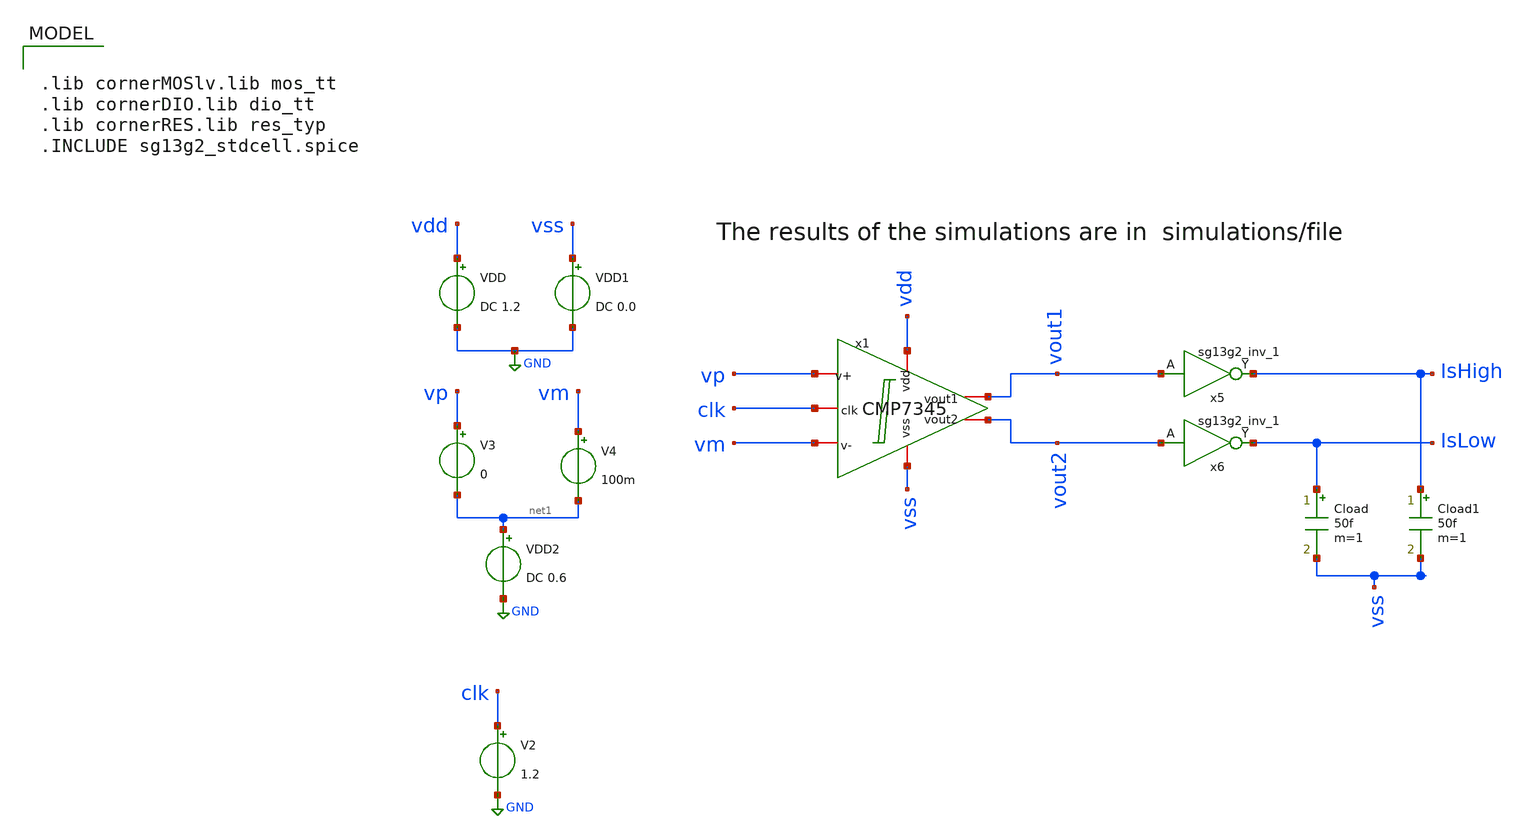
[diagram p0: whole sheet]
** sch_path: CMP7345-main/testbenches/dc/xschem/CMP7345_dc_tb.sch
**.subckt CMP7345_dc_tb
VDD vdd GND DC 1.2
Cload IsLow vss 50f m=1
x1 vdd vout1 vout2 vp vm clk vss CMP7345
VDD1 vss GND DC 0.0
Cload1 IsHigh vss 50f m=1
V2 clk GND 1.2
V3 vp net1 0
VDD2 net1 GND DC 0.6
x5 IsHigh vout1 VDD VSS sg13g2_inv_1
x6 IsLow vout2 VDD VSS sg13g2_inv_1
V4 vm net1 100m
**** begin user architecture code

.lib cornerMOSlv.lib mos_tt
.lib cornerDIO.lib dio_tt
.lib cornerRES.lib res_typ
.INCLUDE sg13g2_stdcell.spice




.options cshunt=20f
.options rseries=1
.control
op
echo " ---------------- Diff pair ----------------" > file
let ids1 = 8*@n.x1.x1.xmb1.nsg13_lv_nmos[ids]
echo Ids1 = $&ids1 >> file
let ids2 = 8*@n.x1.x1.xma1.nsg13_lv_nmos[ids]
echo Ids2 = $&ids2 >> file
let Vgs1 = @n.x1.x1.xmb1.nsg13_lv_nmos[vgs]
echo Vgs1 = $&vgs1 >> file
let Vgs2 = @n.x1.x1.xma1.nsg13_lv_nmos[vgs]
echo Vgs2 = $&vgs2 >> file
let Vth1 = @n.x1.x1.xmb1.nsg13_lv_nmos[vth]
echo Vth1 = $&vth1 >> file
let Vth2 = @n.x1.x1.xma1.nsg13_lv_nmos[vth]
echo Vth2 = $&vth2 >> file
let gm1 = 8*@n.x1.x1.xmb1.nsg13_lv_nmos[gm]
echo gm1 = $&gm1 >> file
let gm2 = 8*@n.x1.x1.xma1.nsg13_lv_nmos[gm]
echo gm2 = $&gm2 >> file
let cdd1 = 8*@n.x1.x1.xmb1.nsg13_lv_nmos[cdd]
echo cdd1 = $&cdd1 >> file
let cdd2 = 8*@n.x1.x1.xma1.nsg13_lv_nmos[cdd]
echo cdd2 = $&cdd2 >> file
let cgg1 = 8*@n.x1.x1.xmb1.nsg13_lv_nmos[cgg]
echo cgg1 = $&cgg1 >> file
let cgg2 = 8*@n.x1.x1.xma1.nsg13_lv_nmos[cgg]
echo cgg2 = $&cgg2 >> file
let css1 = 8*@n.x1.x1.xmb1.nsg13_lv_nmos[css]
echo css1 = $&css1 >> file
let css2 = 8*@n.x1.x1.xma1.nsg13_lv_nmos[css]
echo css2 = $&css2 >> file
echo " ---------------- Tail switch ----------------" >> file
let ids = @n.x1.xm7.nsg13_lv_nmos[ids]
echo Ids = $&ids >> file
let vgs = @n.x1.xm7.nsg13_lv_nmos[vgs]
echo Vgs = $&vgs >> file
let vth = @n.x1.xm7.nsg13_lv_nmos[vth]
echo Vth = $&vth >> file
let gm = @n.x1.xm7.nsg13_lv_nmos[gm]
echo gm = $&gm >> file
let cdd = @n.x1.xm7.nsg13_lv_nmos[cdd]
echo cdd = $&cdd >> file
let cgg = @n.x1.xm7.nsg13_lv_nmos[cgg]
echo cgg = $&cgg >> file
let css = @n.x1.xm7.nsg13_lv_nmos[css]
echo css = $&css >> file
echo " ---------------- NMOS cross coupled pair ----------------" >> file
let ids1 = 8*@n.x1.x2.xma1.nsg13_lv_nmos[ids]
echo Ids1 = $&ids1 >> file
let ids2 = 8*@n.x1.x2.xmb1.nsg13_lv_nmos[ids]
echo Ids2 = $&ids2 >> file
let vgs1 = @n.x1.x2.xma1.nsg13_lv_nmos[vgs]
echo Vgs1 = $&vgs1 >> file
let vgs2 = @n.x1.x2.xmb1.nsg13_lv_nmos[vgs]
echo Vgs2 = $&vgs2 >> file
let vth1 = @n.x1.x2.xma1.nsg13_lv_nmos[vth]
echo Vth1 = $&vth1 >> file
let vth2 = @n.x1.x2.xmb1.nsg13_lv_nmos[vth]
echo Vth2 = $&vth2 >> file
let gm1 = 8*@n.x1.x2.xma1.nsg13_lv_nmos[gm]
echo gm1 = $&gm1 >> file
let gm2 = 8*@n.x1.x2.xmb1.nsg13_lv_nmos[gm]
echo gm2 = $&gm2 >> file
let cdd1 = 8*@n.x1.x2.xma1.nsg13_lv_nmos[cdd]
echo cdd1 = $&cdd1 >> file
let cdd2 = 8*@n.x1.x2.xmb1.nsg13_lv_nmos[cdd]
echo cdd2 = $&cdd2 >> file
let cgg1 = 8*@n.x1.x2.xma1.nsg13_lv_nmos[cgg]
echo cgg1 = $&cgg1 >> file
let cgg2 = 8*@n.x1.x2.xmb1.nsg13_lv_nmos[cgg]
echo cgg2 = $&cgg2 >> file
let css1 = 8*@n.x1.x2.xma1.nsg13_lv_nmos[css]
echo css1 = $&css1 >> file
let css2 = 8*@n.x1.x2.xmb1.nsg13_lv_nmos[css]
echo css2 = $&css2 >> file
echo " ---------------- PMOS cross coupled pair ----------------" >> file
let ids1 = 4*@n.x1.x3.xma1.nsg13_lv_pmos[ids]
echo Ids1 = $&ids1 >> file
let ids2 = 4*@n.x1.x3.xmb1.nsg13_lv_pmos[ids]
echo Ids2 = $&ids2 >> file
let vgs1 = @n.x1.x3.xma1.nsg13_lv_pmos[vgs]
echo Vgs1 = $&vgs1 >> file
let vgs2 = @n.x1.x3.xmb1.nsg13_lv_pmos[vgs]
echo Vgs2 = $&vgs2 >> file
let vth1 = @n.x1.x3.xma1.nsg13_lv_pmos[vth]
echo Vth1 = $&vth1 >> file
let vth2 = @n.x1.x3.xmb1.nsg13_lv_pmos[vth]
echo Vth2 = $&vth2 >> file
let gm1 = 4*@n.x1.x3.xma1.nsg13_lv_pmos[gm]
echo gm1 = $&gm1 >> file
let gm2 = 4*@n.x1.x3.xmb1.nsg13_lv_pmos[gm]
echo gm2 = $&gm2 >> file
let cdd1 = 4*@n.x1.x3.xma1.nsg13_lv_pmos[cdd]
echo cdd1 = $&cdd1 >> file
let cdd2 = 4*@n.x1.x3.xmb1.nsg13_lv_pmos[cdd]
echo cdd2 = $&cdd2 >> file
let cgg1 = 4*@n.x1.x3.xma1.nsg13_lv_pmos[cgg]
echo cgg1 = $&cgg1 >> file
let cgg2 = 4*@n.x1.x3.xmb1.nsg13_lv_pmos[cgg]
echo cgg2 = $&cgg2 >> file
let css1 = 4*@n.x1.x3.xma1.nsg13_lv_pmos[css]
echo css1 = $&css1 >> file
let css2 = 4*@n.x1.x3.xmb1.nsg13_lv_pmos[css]
echo css2 = $&css2 >> file
echo " ---------------- Switches ----------------" >> file
let ids1 = @n.x1.xms1.nsg13_lv_pmos[ids]
echo Ids1 = $&ids1 >> file
let ids2 = @n.x1.xms2.nsg13_lv_pmos[ids]
echo Ids2 = $&ids2 >> file
let ids3 = @n.x1.xms3.nsg13_lv_pmos[ids]
echo Ids3 = $&ids3 >> file
let ids4 = @n.x1.xms4.nsg13_lv_pmos[ids]
echo Ids4 = $&ids4 >> file
let vgs1 = @n.x1.xms1.nsg13_lv_pmos[vgs]
echo Vgs1 = $&vgs1 >> file
let vgs2 = @n.x1.xms2.nsg13_lv_pmos[vgs]
echo Vgs2 = $&vgs2 >> file
let vgs3 = @n.x1.xms3.nsg13_lv_pmos[vgs]
echo Vgs3 = $&vgs3 >> file
let vgs4 = @n.x1.xms4.nsg13_lv_pmos[vgs]
echo Vgs4 = $&vgs4 >> file
let vth1 = @n.x1.xms1.nsg13_lv_pmos[vth]
echo Vth1 = $&vth1 >> file
let vth2 = @n.x1.xms2.nsg13_lv_pmos[vth]
echo Vth2 = $&vth2 >> file
let vth3 = @n.x1.xms3.nsg13_lv_pmos[vth]
echo Vth3 = $&vth3 >> file
let vth4 = @n.x1.xms4.nsg13_lv_pmos[vth]
echo Vth4 = $&vth4 >> file
let gm1 = @n.x1.xms1.nsg13_lv_pmos[gm]
echo gm1 = $&gm1 >> file
let gm2 = @n.x1.xms2.nsg13_lv_pmos[gm]
echo gm2 = $&gm2 >> file
let gm3 = @n.x1.xms3.nsg13_lv_pmos[gm]
echo gm3 = $&gm3 >> file
let gm4 = @n.x1.xms4.nsg13_lv_pmos[gm]
echo gm4 = $&gm4 >> file
let cdd1 = @n.x1.xms1.nsg13_lv_pmos[cdd]
echo cdd1 = $&cdd1 >> file
let cdd2 = @n.x1.xms2.nsg13_lv_pmos[cdd]
echo cdd2 = $&cdd2 >> file
let cdd3 = @n.x1.xms3.nsg13_lv_pmos[cdd]
echo cdd3 = $&cdd3 >> file
let cdd4 = @n.x1.xms4.nsg13_lv_pmos[cdd]
echo cdd4 = $&cdd4 >> file
let cgg1 = @n.x1.xms1.nsg13_lv_pmos[cgg]
echo cgg1 = $&cgg1 >> file
let cgg2 = @n.x1.xms2.nsg13_lv_pmos[cgg]
echo cgg2 = $&cgg2 >> file
let cgg3 = @n.x1.xms3.nsg13_lv_pmos[cgg]
echo cgg3 = $&cgg3 >> file
let cgg4 = @n.x1.xms4.nsg13_lv_pmos[cgg]
echo cgg4 = $&cgg4 >> file
let css1 = @n.x1.xms1.nsg13_lv_pmos[css]
echo css1 = $&css1 >> file
let css2 = @n.x1.xms2.nsg13_lv_pmos[css]
echo css2 = $&css2 >> file
let css3 = @n.x1.xms3.nsg13_lv_pmos[css]
echo css3 = $&css3 >> file
let css4 = @n.x1.xms4.nsg13_lv_pmos[css]
echo css4 = $&css4 >> file
.endc



**** end user architecture code
**.ends

* expanding   symbol:  sg13g2_stdcells/sg13g2_inv_1.sym # of pins=2
** sym_path: sg13g2_stdcells/sg13g2_inv_1.sym
** sch_path: sg13g2_stdcells/sg13g2_inv_1.sch
.subckt sg13g2_inv_1 Y A VDD VSS
*.opin Y
*.ipin A
*.iopin VDD
*.iopin VSS
XM1 Y A VSS VSS sg13_lv_nmos w=740.00n l=130.00n ng=1 m=1 mm_ok=1
XM2 Y A VDD VDD sg13_lv_pmos w=1.12u l=130.00n ng=1 m=1 mm_ok=1
.ends

.GLOBAL GND
.end
